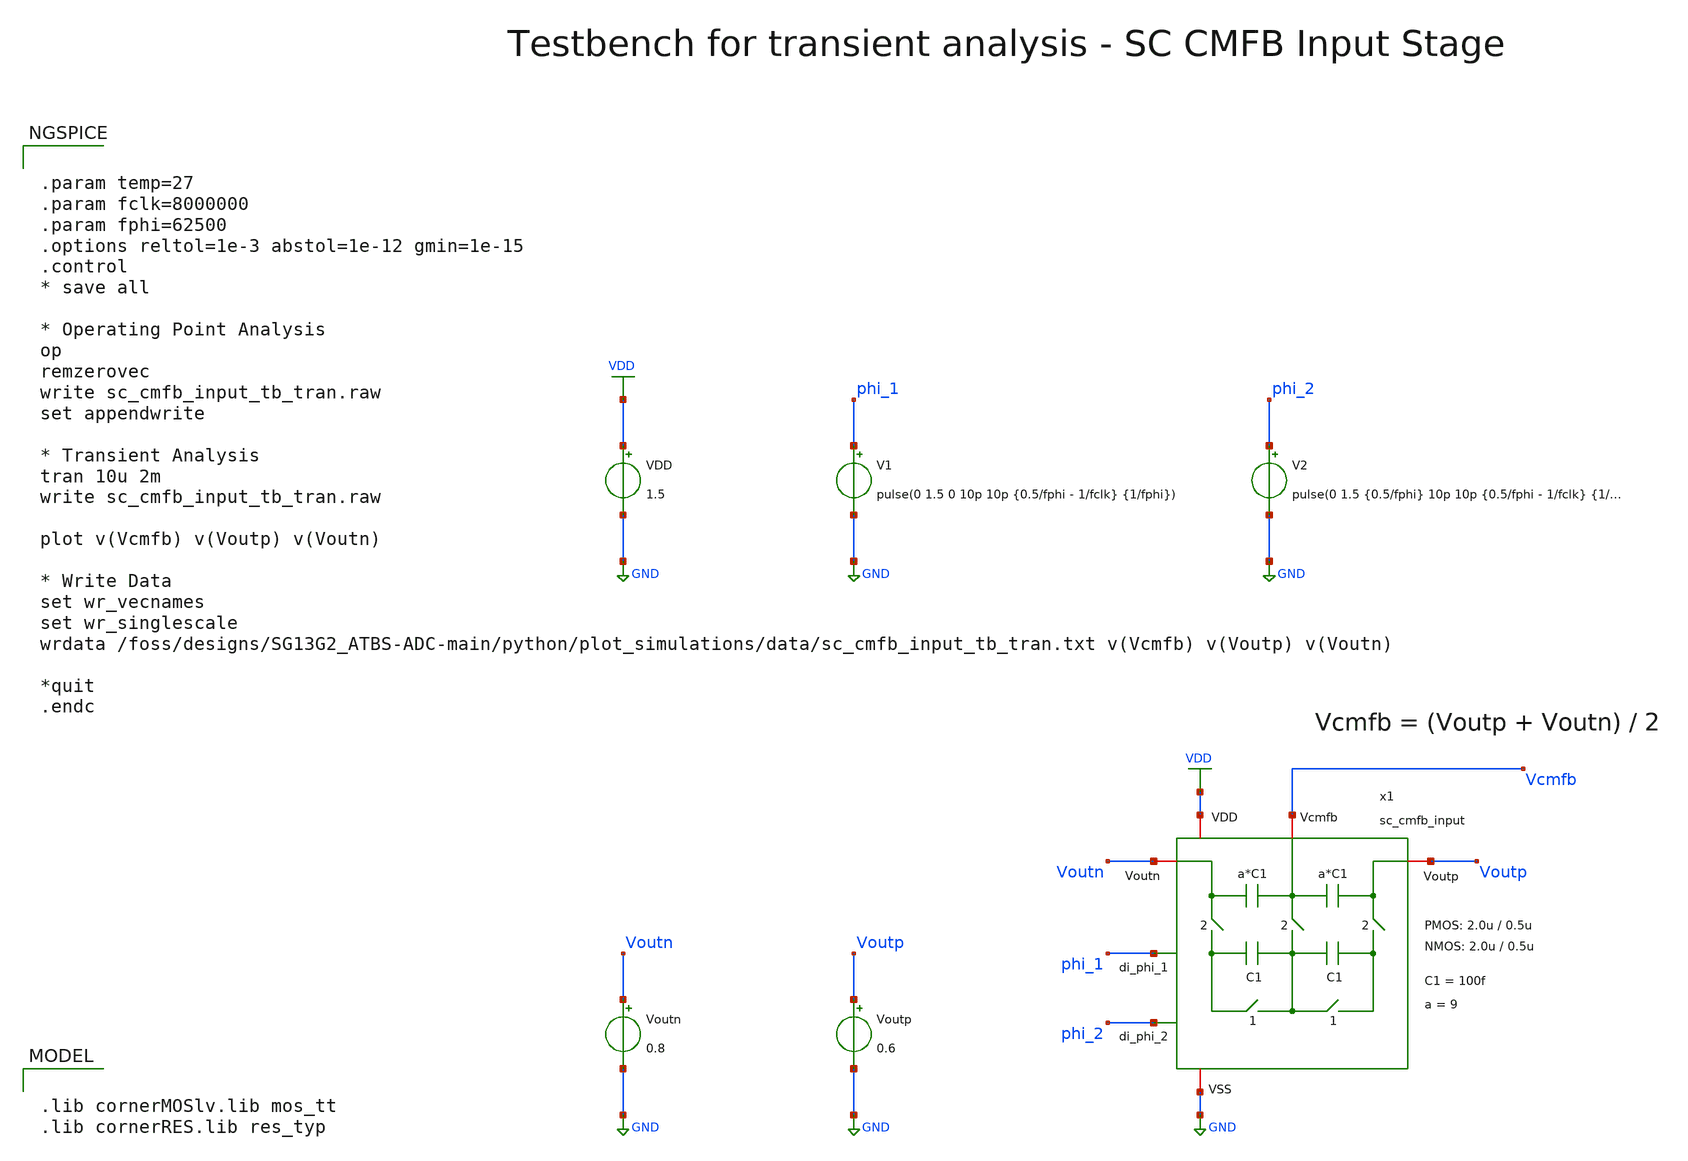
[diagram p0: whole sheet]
** sch_path: SG13G2_ATBS-ADC-main/xschem/bio_amplifier/amplifier_core/sc_cmfb/testbenches/sc_cmfb_input_tb_tran.sch
**.subckt sc_cmfb_input_tb_tran
VDD VDD GND 1.5
V1 phi_1 GND pulse(0 1.5 0 10p 10p {0.5/fphi - 1/fclk} {1/fphi})
V2 phi_2 GND pulse(0 1.5 {0.5/fphi} 10p 10p {0.5/fphi - 1/fclk} {1/fphi})
Voutn Voutn GND 0.8
Voutp Voutp GND 0.6
x1 phi_1 phi_2 VDD Voutp GND Vcmfb Voutn sc_cmfb_input W_P_CMFB=2.0u L_P_CMFB=0.5u W_N_CMFB=2.0u
+ L_N_CMFB=0.5u C1=100f a=9
**** begin user architecture code

.lib cornerMOSlv.lib mos_tt
.lib cornerRES.lib res_typ



.param temp=27
.param fclk=8000000
.param fphi=62500
.options reltol=1e-3 abstol=1e-12 gmin=1e-15
.control
* save all

* Operating Point Analysis
op
remzerovec
write sc_cmfb_input_tb_tran.raw
set appendwrite

* Transient Analysis
tran 10u 2m
write sc_cmfb_input_tb_tran.raw

plot v(Vcmfb) v(Voutp) v(Voutn)

* Write Data
set wr_vecnames
set wr_singlescale
wrdata /foss/designs/SG13G2_ATBS-ADC-main/python/plot_simulations/data/sc_cmfb_input_tb_tran.txt
+ v(Vcmfb) v(Voutp) v(Voutn)

*quit
.endc

**** end user architecture code
**.ends

* expanding   symbol:  bio_amplifier/amplifier_core/sc_cmfb/sc_cmfb_input.sym # of pins=7
** sym_path: SG13G2_ATBS-ADC-main/xschem/bio_amplifier/amplifier_core/sc_cmfb/sc_cmfb_input.sym
** sch_path: SG13G2_ATBS-ADC-main/xschem/bio_amplifier/amplifier_core/sc_cmfb/sc_cmfb_input.sch
.subckt sc_cmfb_input di_phi_1 di_phi_2 VDD Voutp VSS Vcmfb Voutn  W_P_CMFB=2.0u L_P_CMFB=0.5u
+ W_N_CMFB=2.0u L_N_CMFB=0.5u C1=100f a=9
*.iopin VSS
*.iopin VDD
*.iopin Vcmfb
*.iopin Voutp
*.iopin Voutn
*.ipin di_phi_1
*.ipin di_phi_2
x1 VDD di_phi_2 VSS net1 Voutp di_phi_2_n transmission_gate_lv_wo_dummy W_P=W_P_CMFB L_P=L_P_CMFB
+ W_N=W_N_CMFB L_N=L_N_CMFB
C1 Voutp Vcmfb {a*C1} m=1
x2 VDD di_phi_2 VSS net2 Vcmfb di_phi_2_n transmission_gate_lv_wo_dummy W_P=W_P_CMFB L_P=L_P_CMFB
+ W_N=W_N_CMFB L_N=L_N_CMFB
x3 VDD di_phi_2 VSS net3 Voutn di_phi_2_n transmission_gate_lv_wo_dummy W_P=W_P_CMFB L_P=L_P_CMFB
+ W_N=W_N_CMFB L_N=L_N_CMFB
x4 VDD di_phi_1 VSS net2 net1 di_phi_1_n transmission_gate_lv_wo_dummy W_P=W_P_CMFB L_P=L_P_CMFB
+ W_N=W_N_CMFB L_N=L_N_CMFB
x5 VDD di_phi_1 VSS net2 net3 di_phi_1_n transmission_gate_lv_wo_dummy W_P=W_P_CMFB L_P=L_P_CMFB
+ W_N=W_N_CMFB L_N=L_N_CMFB
C2 Vcmfb Voutn {a*C1} m=1
C3 net1 net2 C1 m=1
C4 net2 net3 C1 m=1
x7 VDD di_phi_1 di_phi_1_n VSS inverter_lv W_P=W_P_CMFB L_P=L_P_CMFB W_N=W_N_CMFB L_N=L_N_CMFB
x6 VDD di_phi_2 di_phi_2_n VSS inverter_lv W_P=W_P_CMFB L_P=L_P_CMFB W_N=W_N_CMFB L_N=L_N_CMFB
.ends


* expanding   symbol:  transmission_gate/transmission_gate_lv_wo_dummy.sym # of pins=6
** sym_path: SG13G2_ATBS-ADC-main/xschem/transmission_gate/transmission_gate_lv_wo_dummy.sym
** sch_path: SG13G2_ATBS-ADC-main/xschem/transmission_gate/transmission_gate_lv_wo_dummy.sch
.subckt transmission_gate_lv_wo_dummy VDD di_tg_ctrl VSS v_b v_a di_tg_ctrl_n  W_P=1.0u L_P=0.13u
+ W_N=1.0u L_N=0.13u
*.iopin v_a
*.iopin v_b
*.iopin VDD
*.iopin VSS
*.ipin di_tg_ctrl
*.ipin di_tg_ctrl_n
XM1 v_a di_tg_ctrl v_b VSS sg13_lv_nmos w=W_N l=L_N ng=1 m=1 mm_ok=1
XM2 v_a di_tg_ctrl_n v_b VDD sg13_lv_pmos w=W_P l=L_P ng=1 m=1 mm_ok=1
.ends


* expanding   symbol:  inverter/inverter_lv.sym # of pins=4
** sym_path: SG13G2_ATBS-ADC-main/xschem/inverter/inverter_lv.sym
** sch_path: SG13G2_ATBS-ADC-main/xschem/inverter/inverter_lv.sch
.subckt inverter_lv VDD vin vout VSS  W_P=3.0u L_P=0.13u W_N=1.0u L_N=0.13u
*.ipin vin
*.iopin VDD
*.iopin VSS
*.opin vout
XM1 vout vin VDD VDD sg13_lv_pmos w=W_P l=L_P ng=1 m=1 mm_ok=1
XM2 vout vin VSS VSS sg13_lv_nmos w=W_N l=L_N ng=1 m=1 mm_ok=1
.ends

.GLOBAL GND
.GLOBAL VDD
.end
